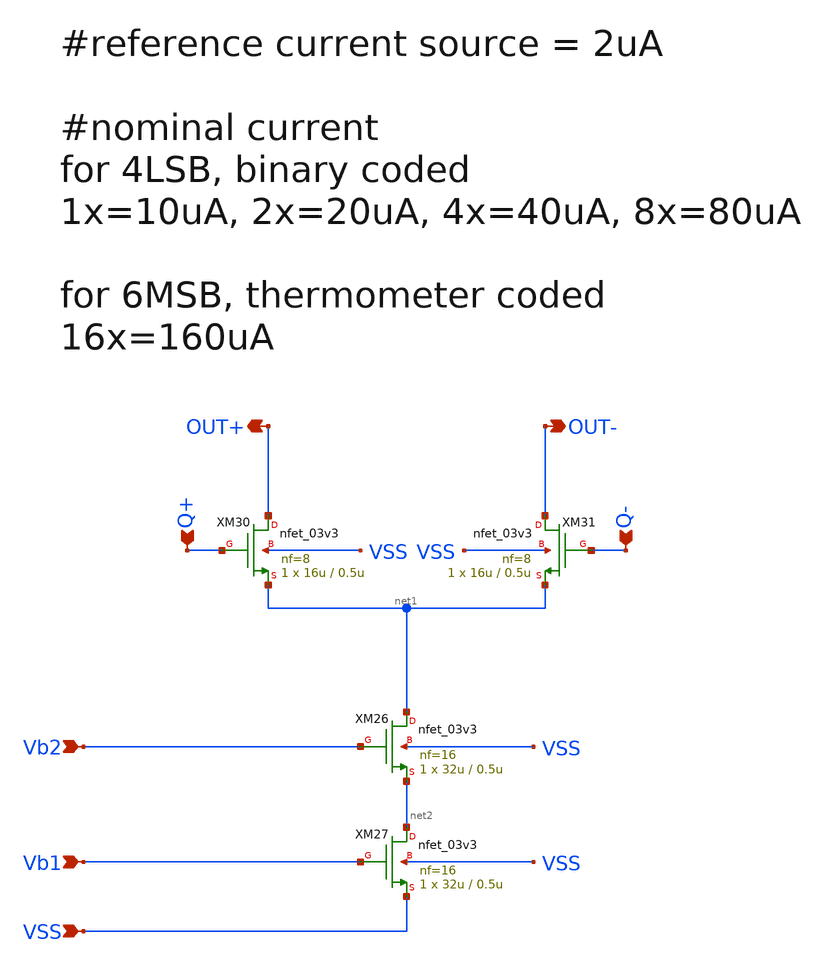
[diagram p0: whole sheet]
** sch_path: DAC/xschem/dac_msb_analog.sch
**.subckt dac_msb_analog Q- Q+ Vb1 Vb2 OUT+ OUT- VSS
*.ipin Q-
*.ipin Q+
*.ipin Vb1
*.ipin Vb2
*.opin OUT+
*.opin OUT-
*.ipin VSS
XM26 net1 Vb2 net2 VSS nfet_03v3 L=0.5u W=32u nf=16 ad='int((nf+1)/2) * W/nf * 0.18u' as='int((nf+2)/2) * W/nf * 0.18u'
+ pd='2*int((nf+1)/2) * (W/nf + 0.18u)' ps='2*int((nf+2)/2) * (W/nf + 0.18u)' nrd='0.18u / W' nrs='0.18u / W'
+ sa=0 sb=0 sd=0 m=1
XM27 net2 Vb1 VSS VSS nfet_03v3 L=0.5u W=32u nf=16 ad='int((nf+1)/2) * W/nf * 0.18u' as='int((nf+2)/2) * W/nf * 0.18u'
+ pd='2*int((nf+1)/2) * (W/nf + 0.18u)' ps='2*int((nf+2)/2) * (W/nf + 0.18u)' nrd='0.18u / W' nrs='0.18u / W'
+ sa=0 sb=0 sd=0 m=1
XM30 OUT+ Q+ net1 VSS nfet_03v3 L=0.5u W=16u nf=8 ad='int((nf+1)/2) * W/nf * 0.18u' as='int((nf+2)/2) * W/nf * 0.18u'
+ pd='2*int((nf+1)/2) * (W/nf + 0.18u)' ps='2*int((nf+2)/2) * (W/nf + 0.18u)' nrd='0.18u / W' nrs='0.18u / W'
+ sa=0 sb=0 sd=0 m=1
XM31 OUT- Q- net1 VSS nfet_03v3 L=0.5u W=16u nf=8 ad='int((nf+1)/2) * W/nf * 0.18u' as='int((nf+2)/2) * W/nf * 0.18u'
+ pd='2*int((nf+1)/2) * (W/nf + 0.18u)' ps='2*int((nf+2)/2) * (W/nf + 0.18u)' nrd='0.18u / W' nrs='0.18u / W'
+ sa=0 sb=0 sd=0 m=1
**.ends
.end
